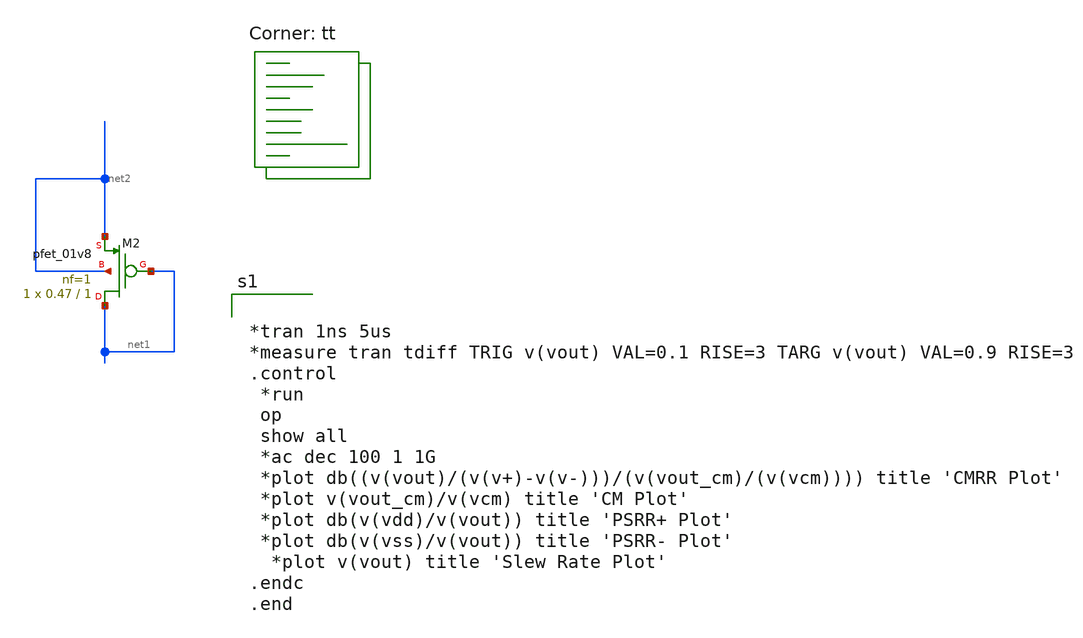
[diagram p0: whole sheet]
** sch_path: xschem/untitled-2.sch
**.subckt untitled-2
XM2 net1 net1 net2 net2 sky130_fd_pr__pfet_01v8 L=1 W=0.47 nf=1 ad='int((1 + 1)/2) * 0.47 / 1 * 0.29'
+ as='int((1 + 2)/2) * 0.47 / 1 * 0.29' pd='2*int((1 + 1)/2) * (0.47 / 1 + 0.29)' ps='2*int((1 + 2)/2) * (0.47 / 1 + 0.29)'
+ nrd='0.29 / 0.47 ' nrs='0.29 / 0.47 ' sa=0 sb=0 sd=0 mult=1 m=1
**** begin user architecture code
.lib $::SKYWATER_MODELS/sky130.lib.spice tt


*tran 1ns 5us
*measure tran tdiff TRIG v(vout) VAL=0.1 RISE=3 TARG v(vout) VAL=0.9 RISE=3
.control
 *run
 op
 show all
 *ac dec 100 1 1G
 *plot db((v(vout)/(v(v+)-v(v-)))/(v(vout_cm)/(v(vcm)))) title 'CMRR Plot'
 *plot v(vout_cm)/v(vcm) title 'CM Plot'
 *plot db(v(vdd)/v(vout)) title 'PSRR+ Plot'
 *plot db(v(vss)/v(vout)) title 'PSRR- Plot'
  *plot v(vout) title 'Slew Rate Plot'
.endc
.end

**** end user architecture code
**.ends
.end
